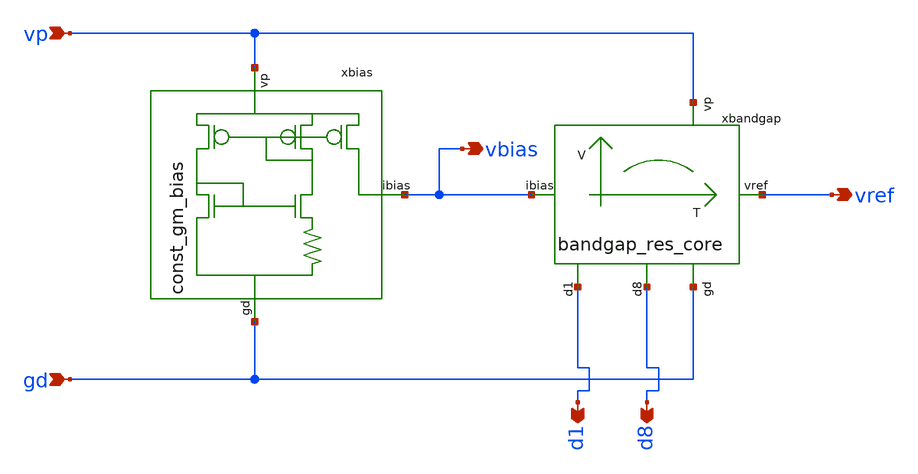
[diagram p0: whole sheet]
** sch_path: circuit/bandgap_res_core_wrapper.sch
**.subckt bandgap_res_core_wrapper vp gd vref d1 d8 vbias
*.ipin vp
*.ipin gd
*.opin vref
*.opin d1
*.opin d8
*.opin vbias
xbandgap vp vbias vref gd d8 d1 bandgap_res_core
xbias vp vbias gd const_gm_bias
**.ends
.end
